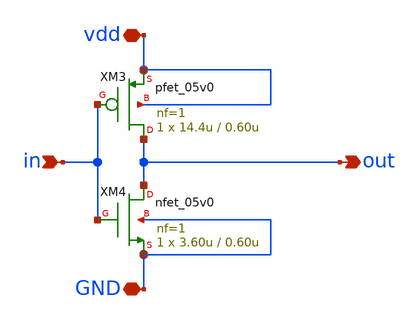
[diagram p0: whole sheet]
** sch_path: member_project/ponzu840w/inv/inv.sch
**.subckt inv GND vdd in out
*.iopin GND
*.iopin vdd
*.ipin in
*.opin out
XM3 out in vdd vdd pfet_05v0 L=0.60u W=14.4u nf=1 ad='int((nf+1)/2) * W/nf * 0.18u' as='int((nf+2)/2) * W/nf * 0.18u'
+ pd='2*int((nf+1)/2) * (W/nf + 0.18u)' ps='2*int((nf+2)/2) * (W/nf + 0.18u)' nrd='0.18u / W' nrs='0.18u / W'
+ sa=0 sb=0 sd=0 m=1
XM4 out in GND GND nfet_05v0 L=0.60u W=3.60u nf=1 ad='int((nf+1)/2) * W/nf * 0.18u' as='int((nf+2)/2) * W/nf * 0.18u'
+ pd='2*int((nf+1)/2) * (W/nf + 0.18u)' ps='2*int((nf+2)/2) * (W/nf + 0.18u)' nrd='0.18u / W' nrs='0.18u / W'
+ sa=0 sb=0 sd=0 m=1
**.ends
.end
